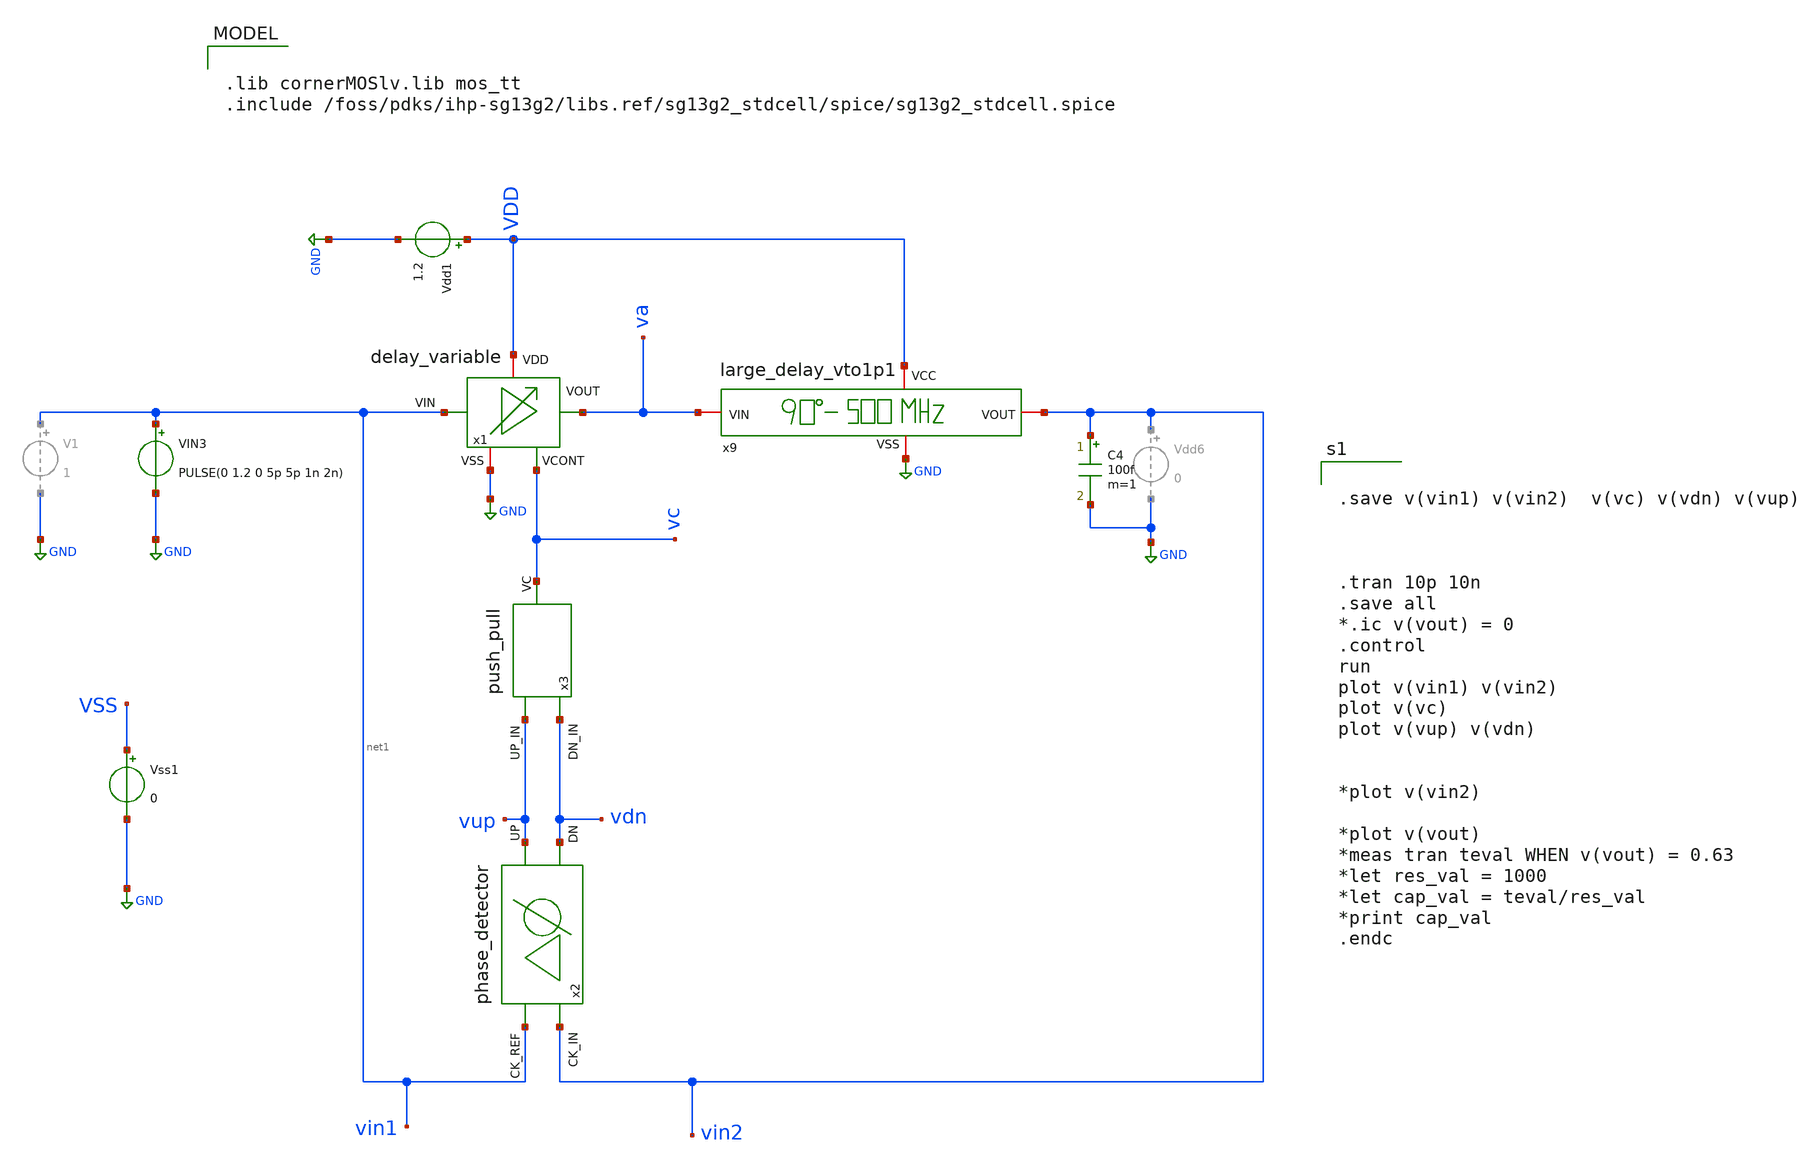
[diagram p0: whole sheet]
** sch_path: sch/DLL/DLL_tb.sch
**.subckt DLL_tb
Vdd1 VDD GND 1.2
x1 VDD net1 va vc GND delay_variable
C4 vin2 GND 100f m=1
VIN3 net1 GND PULSE(0 1.2 0 5p 5p 1n 2n)
x9 VDD GND va vin2 large_delay_vto1p1
Vss1 VSS GND 0
x2 vin2 net2 net1 vdn phase_detector
x3 vup net3 vdn push_pull
**** begin user architecture code


.save v(vin1) v(vin2)  v(vc) v(vdn) v(vup)



.tran 10p 10n
.save all
*.ic v(vout) = 0
.control
run
plot v(vin1) v(vin2)
plot v(vc)
plot v(vup) v(vdn)


*plot v(vin2)

*plot v(vout)
*meas tran teval WHEN v(vout) = 0.63
*let res_val = 1000
*let cap_val = teval/res_val
*print cap_val
.endc



.lib cornerMOSlv.lib mos_tt
.include /foss/pdks/ihp-sg13g2/libs.ref/sg13g2_stdcell/spice/sg13g2_stdcell.spice

**** end user architecture code
**.ends
.GLOBAL GND
.end
